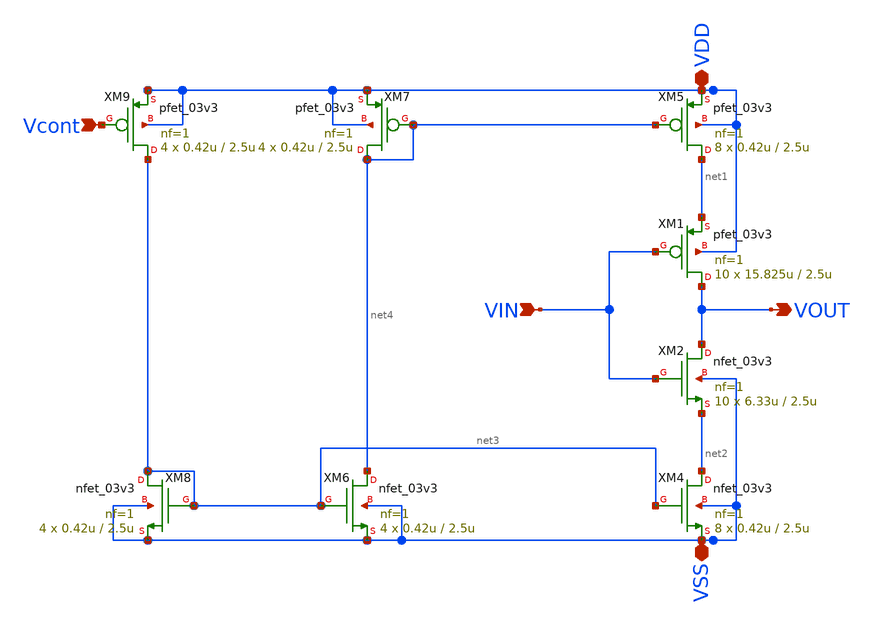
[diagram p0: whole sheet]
** sch_path: ABC123_SDC/design_data/klayout/OSC/OSC_INV/OSC_INV.sch
**.subckt OSC_INV VIN VOUT VDD VSS Vcont
*.ipin VIN
*.opin VOUT
*.iopin VDD
*.iopin VSS
*.ipin Vcont
XM4 net2 net3 VSS VSS nfet_03v3 L=2.5u W=0.42u nf=1 ad='int((nf+1)/2) * W/nf * 0.18u' as='int((nf+2)/2) * W/nf * 0.18u'
+ pd='2*int((nf+1)/2) * (W/nf + 0.18u)' ps='2*int((nf+2)/2) * (W/nf + 0.18u)' nrd='0.18u / W' nrs='0.18u / W'
+ sa=0 sb=0 sd=0 m=8
XM5 net1 net4 VDD VDD pfet_03v3 L=2.5u W=0.42u nf=1 ad='int((nf+1)/2) * W/nf * 0.18u' as='int((nf+2)/2) * W/nf * 0.18u'
+ pd='2*int((nf+1)/2) * (W/nf + 0.18u)' ps='2*int((nf+2)/2) * (W/nf + 0.18u)' nrd='0.18u / W' nrs='0.18u / W'
+ sa=0 sb=0 sd=0 m=8
XM6 net4 net3 VSS VSS nfet_03v3 L=2.5u W=0.42u nf=1 ad='int((nf+1)/2) * W/nf * 0.18u' as='int((nf+2)/2) * W/nf * 0.18u'
+ pd='2*int((nf+1)/2) * (W/nf + 0.18u)' ps='2*int((nf+2)/2) * (W/nf + 0.18u)' nrd='0.18u / W' nrs='0.18u / W'
+ sa=0 sb=0 sd=0 m=4
XM7 net4 net4 VDD VDD pfet_03v3 L=2.5u W=0.42u nf=1 ad='int((nf+1)/2) * W/nf * 0.18u' as='int((nf+2)/2) * W/nf * 0.18u'
+ pd='2*int((nf+1)/2) * (W/nf + 0.18u)' ps='2*int((nf+2)/2) * (W/nf + 0.18u)' nrd='0.18u / W' nrs='0.18u / W'
+ sa=0 sb=0 sd=0 m=4
XM8 net3 net3 VSS VSS nfet_03v3 L=2.5u W=0.42u nf=1 ad='int((nf+1)/2) * W/nf * 0.18u' as='int((nf+2)/2) * W/nf * 0.18u'
+ pd='2*int((nf+1)/2) * (W/nf + 0.18u)' ps='2*int((nf+2)/2) * (W/nf + 0.18u)' nrd='0.18u / W' nrs='0.18u / W'
+ sa=0 sb=0 sd=0 m=4
XM9 net3 Vcont VDD VDD pfet_03v3 L=2.5u W=0.42u nf=1 ad='int((nf+1)/2) * W/nf * 0.18u' as='int((nf+2)/2) * W/nf * 0.18u'
+ pd='2*int((nf+1)/2) * (W/nf + 0.18u)' ps='2*int((nf+2)/2) * (W/nf + 0.18u)' nrd='0.18u / W' nrs='0.18u / W'
+ sa=0 sb=0 sd=0 m=4
XM1 VOUT VIN net1 VDD pfet_03v3 L=2.5u W=15.825u nf=1 ad='int((nf+1)/2) * W/nf * 0.18u' as='int((nf+2)/2) * W/nf * 0.18u'
+ pd='2*int((nf+1)/2) * (W/nf + 0.18u)' ps='2*int((nf+2)/2) * (W/nf + 0.18u)' nrd='0.18u / W' nrs='0.18u / W'
+ sa=0 sb=0 sd=0 m=10
XM2 VOUT VIN net2 VSS nfet_03v3 L=2.5u W=6.33u nf=1 ad='int((nf+1)/2) * W/nf * 0.18u' as='int((nf+2)/2) * W/nf * 0.18u'
+ pd='2*int((nf+1)/2) * (W/nf + 0.18u)' ps='2*int((nf+2)/2) * (W/nf + 0.18u)' nrd='0.18u / W' nrs='0.18u / W'
+ sa=0 sb=0 sd=0 m=10
**.ends
.end
